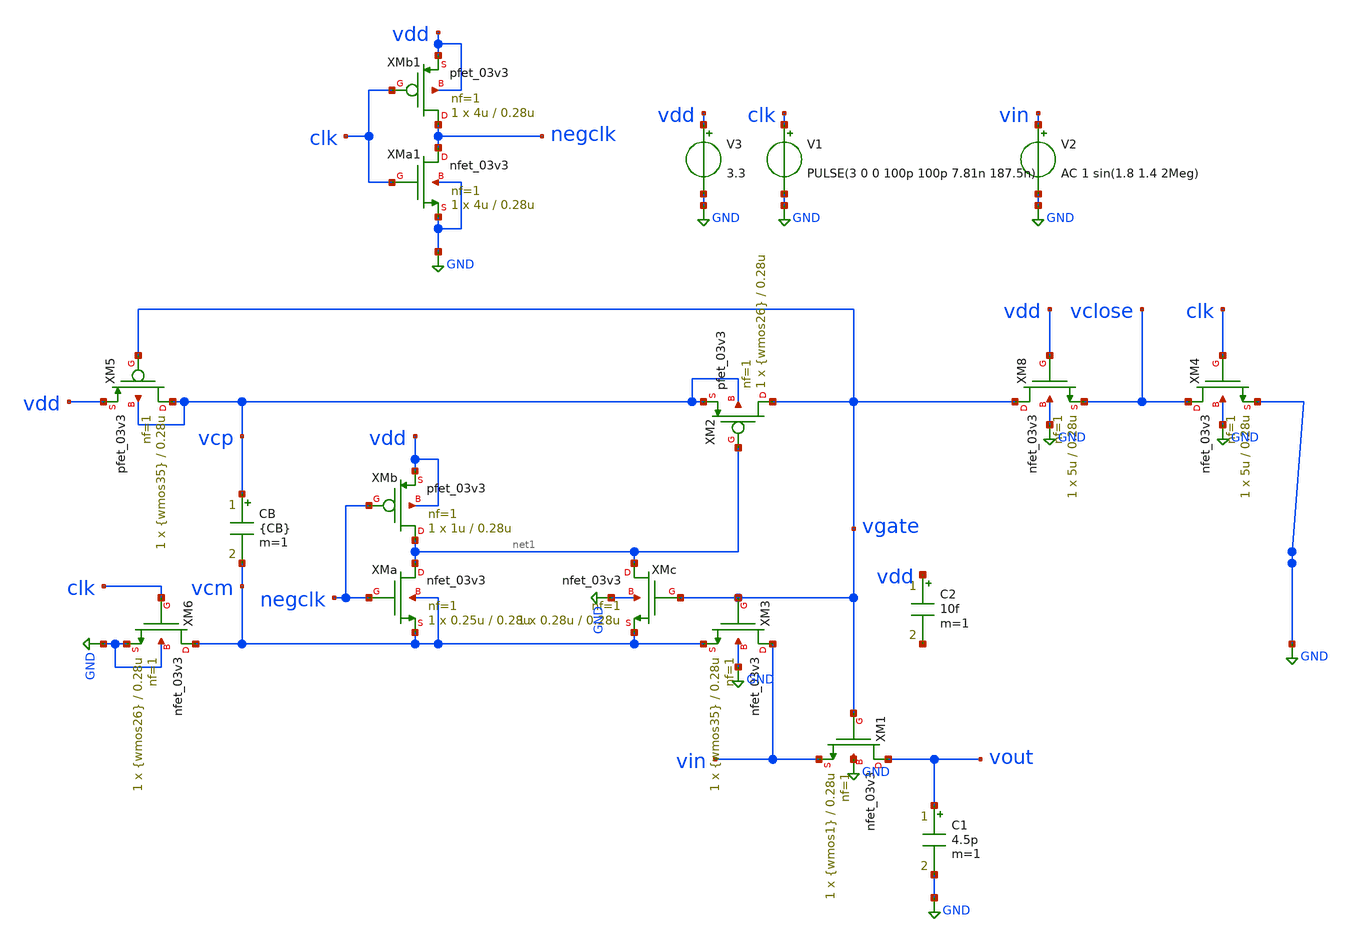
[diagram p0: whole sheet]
** sch_path: SAR_ADC/xschem/designs/sw_design/bootstrap_sw_design.sch
**.subckt bootstrap_sw_design
XM1 vout vgate vin GND nfet_03v3 L=0.28u W={wmos1} nf=1 ad='int((nf+1)/2) * W/nf * 0.18u' as='int((nf+2)/2) * W/nf * 0.18u'
+ pd='2*int((nf+1)/2) * (W/nf + 0.18u)' ps='2*int((nf+2)/2) * (W/nf + 0.18u)' nrd='0.18u / W' nrs='0.18u / W'
+ sa=0 sb=0 sd=0 m=1
XM2 vgate net1 vcp vcp pfet_03v3 L=0.28u W={wmos26} nf=1 ad='int((nf+1)/2) * W/nf * 0.18u' as='int((nf+2)/2) * W/nf * 0.18u'
+ pd='2*int((nf+1)/2) * (W/nf + 0.18u)' ps='2*int((nf+2)/2) * (W/nf + 0.18u)' nrd='0.18u / W' nrs='0.18u / W'
+ sa=0 sb=0 sd=0 m=1
XM3 vin vgate vcm GND nfet_03v3 L=0.28u W={wmos35} nf=1 ad='int((nf+1)/2) * W/nf * 0.18u' as='int((nf+2)/2) * W/nf * 0.18u'
+ pd='2*int((nf+1)/2) * (W/nf + 0.18u)' ps='2*int((nf+2)/2) * (W/nf + 0.18u)' nrd='0.18u / W' nrs='0.18u / W'
+ sa=0 sb=0 sd=0 m=1
XM8 vgate vdd vclose GND nfet_03v3 L=0.28u W=5u nf=1 ad='int((nf+1)/2) * W/nf * 0.18u' as='int((nf+2)/2) * W/nf * 0.18u'
+ pd='2*int((nf+1)/2) * (W/nf + 0.18u)' ps='2*int((nf+2)/2) * (W/nf + 0.18u)' nrd='0.18u / W' nrs='0.18u / W'
+ sa=0 sb=0 sd=0 m=1
XM6 vcm clk GND GND nfet_03v3 L=0.28u W={wmos26} nf=1 ad='int((nf+1)/2) * W/nf * 0.18u' as='int((nf+2)/2) * W/nf * 0.18u'
+ pd='2*int((nf+1)/2) * (W/nf + 0.18u)' ps='2*int((nf+2)/2) * (W/nf + 0.18u)' nrd='0.18u / W' nrs='0.18u / W'
+ sa=0 sb=0 sd=0 m=1
XM4 vclose clk GND GND nfet_03v3 L=0.28u W=5u nf=1 ad='int((nf+1)/2) * W/nf * 0.18u' as='int((nf+2)/2) * W/nf * 0.18u'
+ pd='2*int((nf+1)/2) * (W/nf + 0.18u)' ps='2*int((nf+2)/2) * (W/nf + 0.18u)' nrd='0.18u / W' nrs='0.18u / W'
+ sa=0 sb=0 sd=0 m=1
XM5 vcp vgate vdd vcp pfet_03v3 L=0.28u W={wmos35} nf=1 ad='int((nf+1)/2) * W/nf * 0.18u' as='int((nf+2)/2) * W/nf * 0.18u'
+ pd='2*int((nf+1)/2) * (W/nf + 0.18u)' ps='2*int((nf+2)/2) * (W/nf + 0.18u)' nrd='0.18u / W' nrs='0.18u / W'
+ sa=0 sb=0 sd=0 m=1
V1 clk GND PULSE(3 0 0 100p 100p 7.81n 187.5n)
V2 vin GND AC 1 sin(1.8 1.4 2Meg)
V3 vdd GND 3.3
C1 vout GND 4.5p m=1
CB vcp vcm {CB} m=1
XMc net1 vgate vcm GND nfet_03v3 L=0.28u W=0.28u nf=1 ad='int((nf+1)/2) * W/nf * 0.18u' as='int((nf+2)/2) * W/nf * 0.18u'
+ pd='2*int((nf+1)/2) * (W/nf + 0.18u)' ps='2*int((nf+2)/2) * (W/nf + 0.18u)' nrd='0.18u / W' nrs='0.18u / W'
+ sa=0 sb=0 sd=0 m=1
XMa net1 negclk vcm vcm nfet_03v3 L=0.28u W=0.25u nf=1 ad='int((nf+1)/2) * W/nf * 0.18u' as='int((nf+2)/2) * W/nf * 0.18u'
+ pd='2*int((nf+1)/2) * (W/nf + 0.18u)' ps='2*int((nf+2)/2) * (W/nf + 0.18u)' nrd='0.18u / W' nrs='0.18u / W'
+ sa=0 sb=0 sd=0 m=1
XMb net1 negclk vdd vdd pfet_03v3 L=0.28u W=1u nf=1 ad='int((nf+1)/2) * W/nf * 0.18u' as='int((nf+2)/2) * W/nf * 0.18u'
+ pd='2*int((nf+1)/2) * (W/nf + 0.18u)' ps='2*int((nf+2)/2) * (W/nf + 0.18u)' nrd='0.18u / W' nrs='0.18u / W'
+ sa=0 sb=0 sd=0 m=1
XMa1 negclk clk GND GND nfet_03v3 L=0.28u W=4u nf=1 ad='int((nf+1)/2) * W/nf * 0.18u' as='int((nf+2)/2) * W/nf * 0.18u'
+ pd='2*int((nf+1)/2) * (W/nf + 0.18u)' ps='2*int((nf+2)/2) * (W/nf + 0.18u)' nrd='0.18u / W' nrs='0.18u / W'
+ sa=0 sb=0 sd=0 m=1
XMb1 negclk clk vdd vdd pfet_03v3 L=0.28u W=4u nf=1 ad='int((nf+1)/2) * W/nf * 0.18u' as='int((nf+2)/2) * W/nf * 0.18u'
+ pd='2*int((nf+1)/2) * (W/nf + 0.18u)' ps='2*int((nf+2)/2) * (W/nf + 0.18u)' nrd='0.18u / W' nrs='0.18u / W'
+ sa=0 sb=0 sd=0 m=1
C2 vdd net2 10f m=1
**** begin user architecture code

.include $env(PDK_ROOT)/$env(PDK)/libs.tech/ngspice/design.ngspice
.lib $env(PDK_ROOT)/$env(PDK)/libs.tech/ngspice/sm141064.ngspice typical



.param CB=1p
.param wmos35=3u
.param wmos26=0.28u
.param wmos1=25u
.control


***** for W_MOS M2-M6 *****

*compose wid values 0.28u 1.5u 5u 15u
*foreach widmos $&wid
*alterparam wmos26=$widmos

***** for W_MOS M3-M5 *****

*compose wid values 3u 5u 10u 20u
*foreach widmos $&wid
*alterparam wmos35=$widmos

***** for W_MOS M1 *****

*compose wid values 8u 10u 15u 20u
*foreach widmos $&wid
*alterparam wmos1=$widmos

*reset

save all
tran 50p 5u 3u
*wrdata /foss/designs/sw_comp_gf180/bootstrap_switch/data/data_vout_m26.dat vin vout
*set appendwrite
*end

*plot vclose
plot vin vout clk

*plot vgate vin

***** For AC analysis *****

*ac dec 200 10 1000Meg
*settype decibel vout
*plot vdb(vout)
*op
.endc

**** end user architecture code
**.ends
.GLOBAL GND
.end
